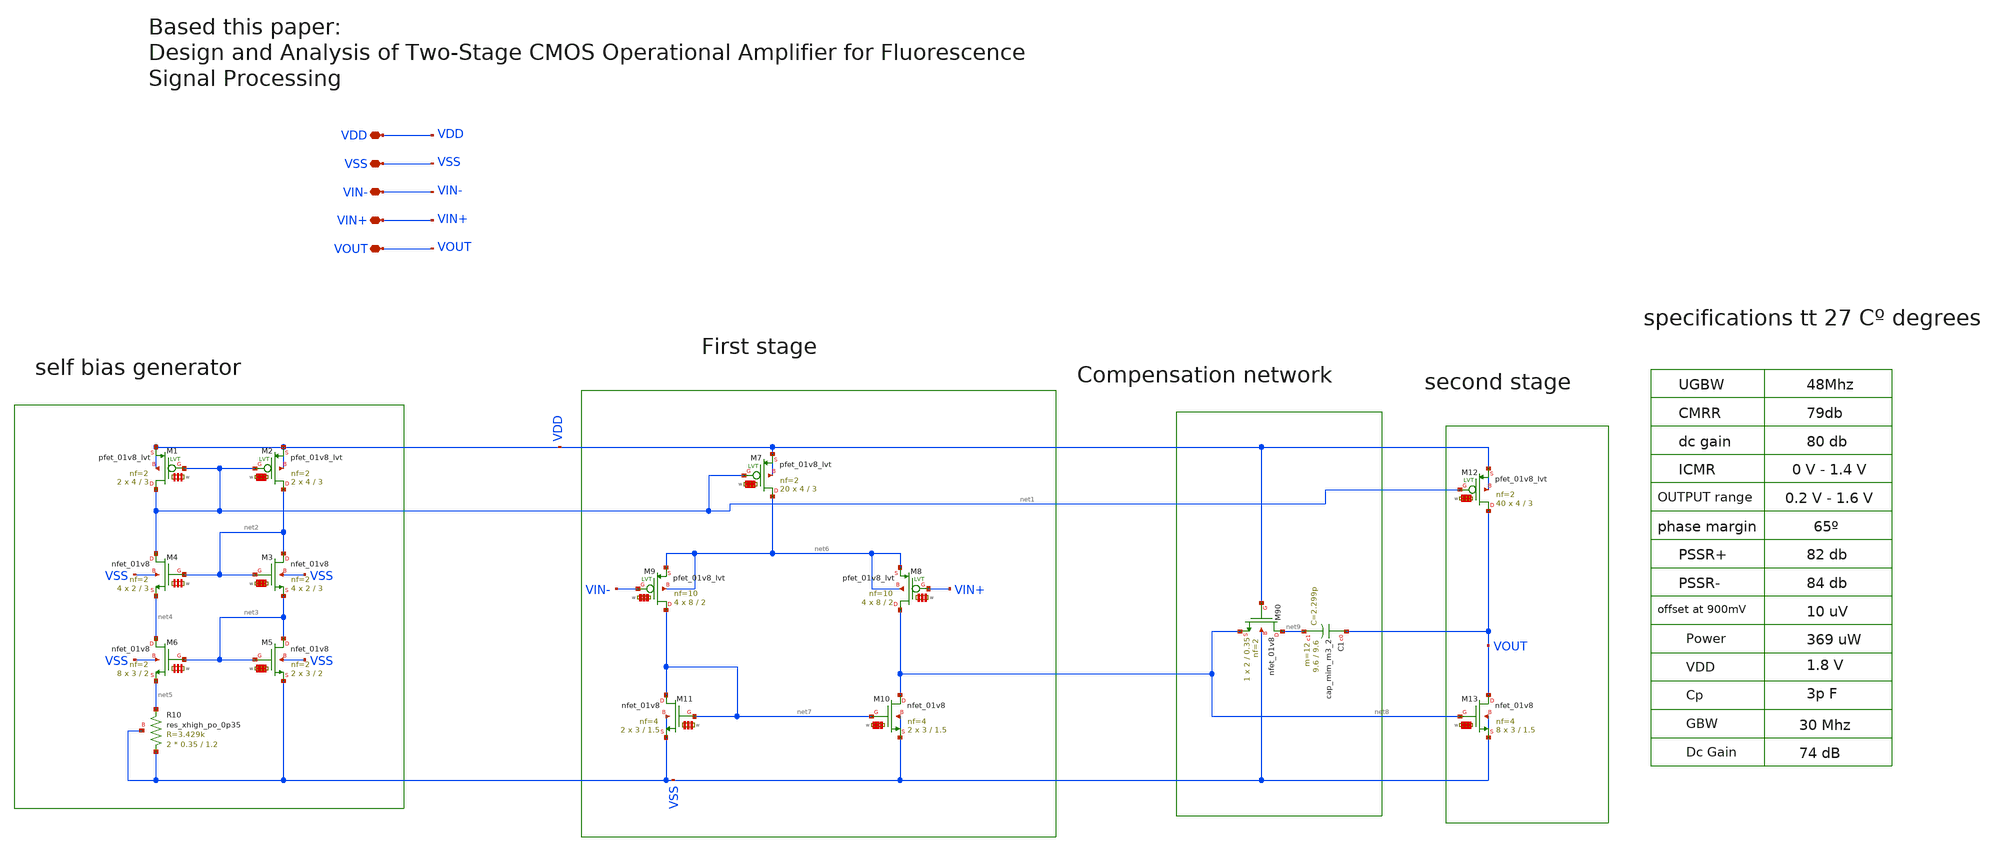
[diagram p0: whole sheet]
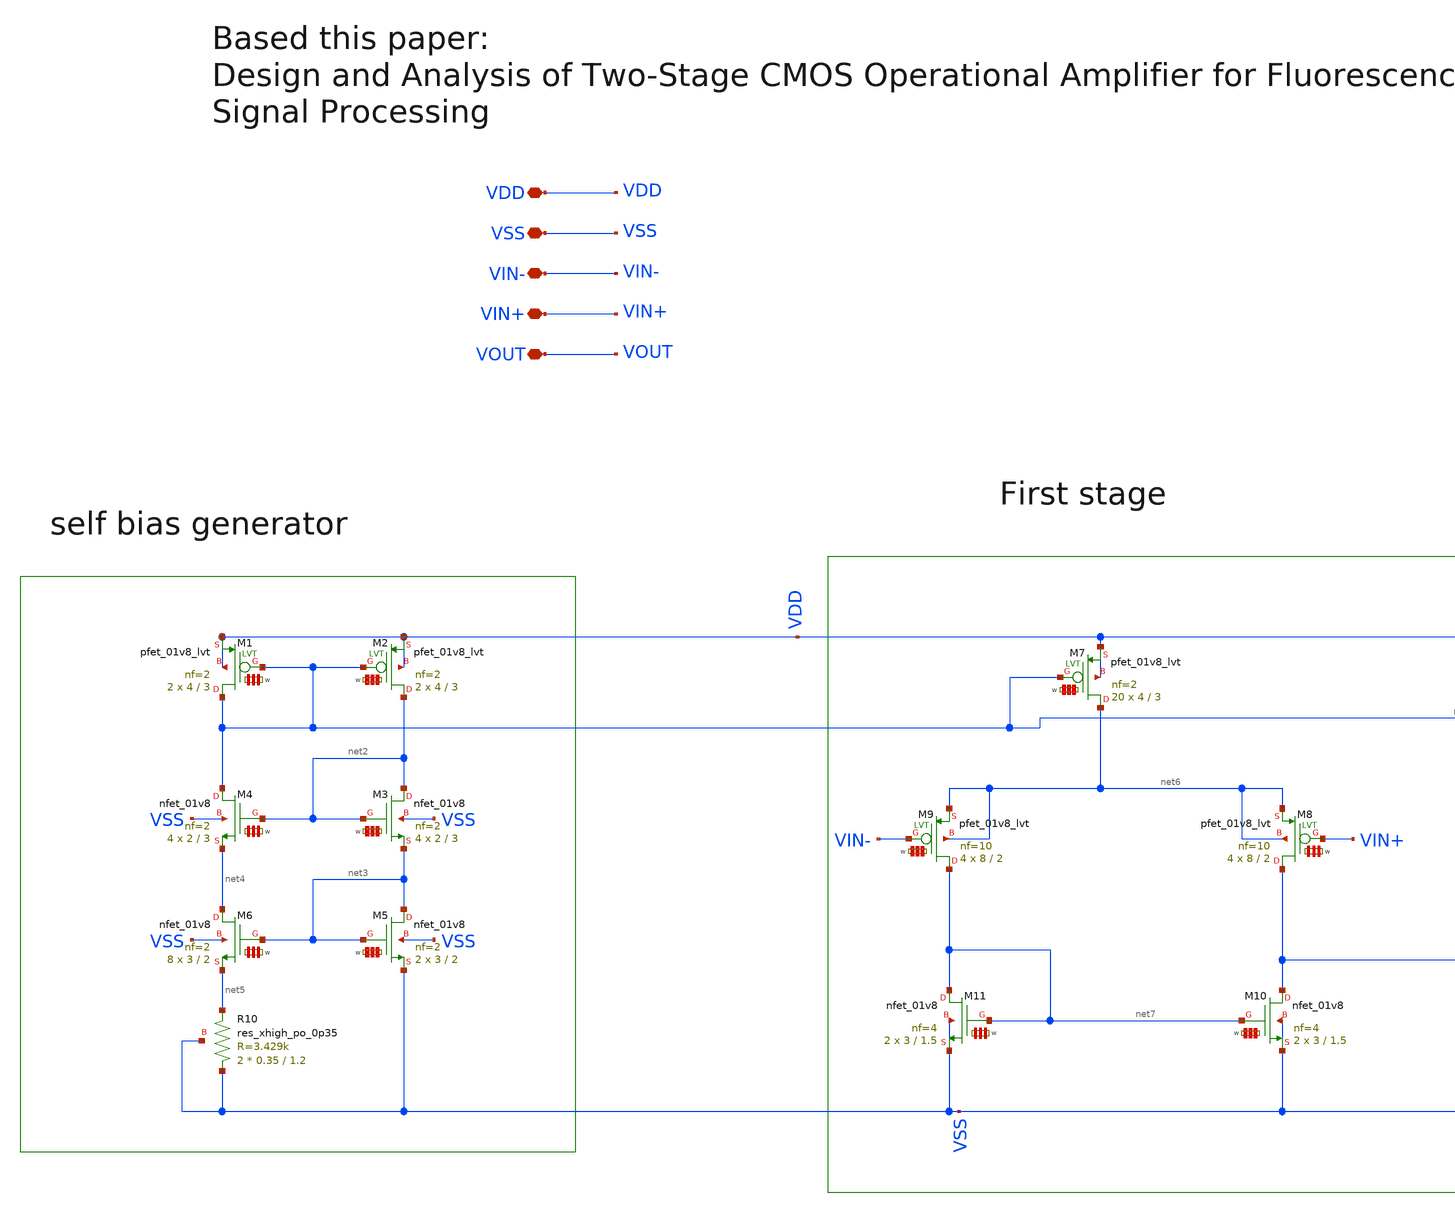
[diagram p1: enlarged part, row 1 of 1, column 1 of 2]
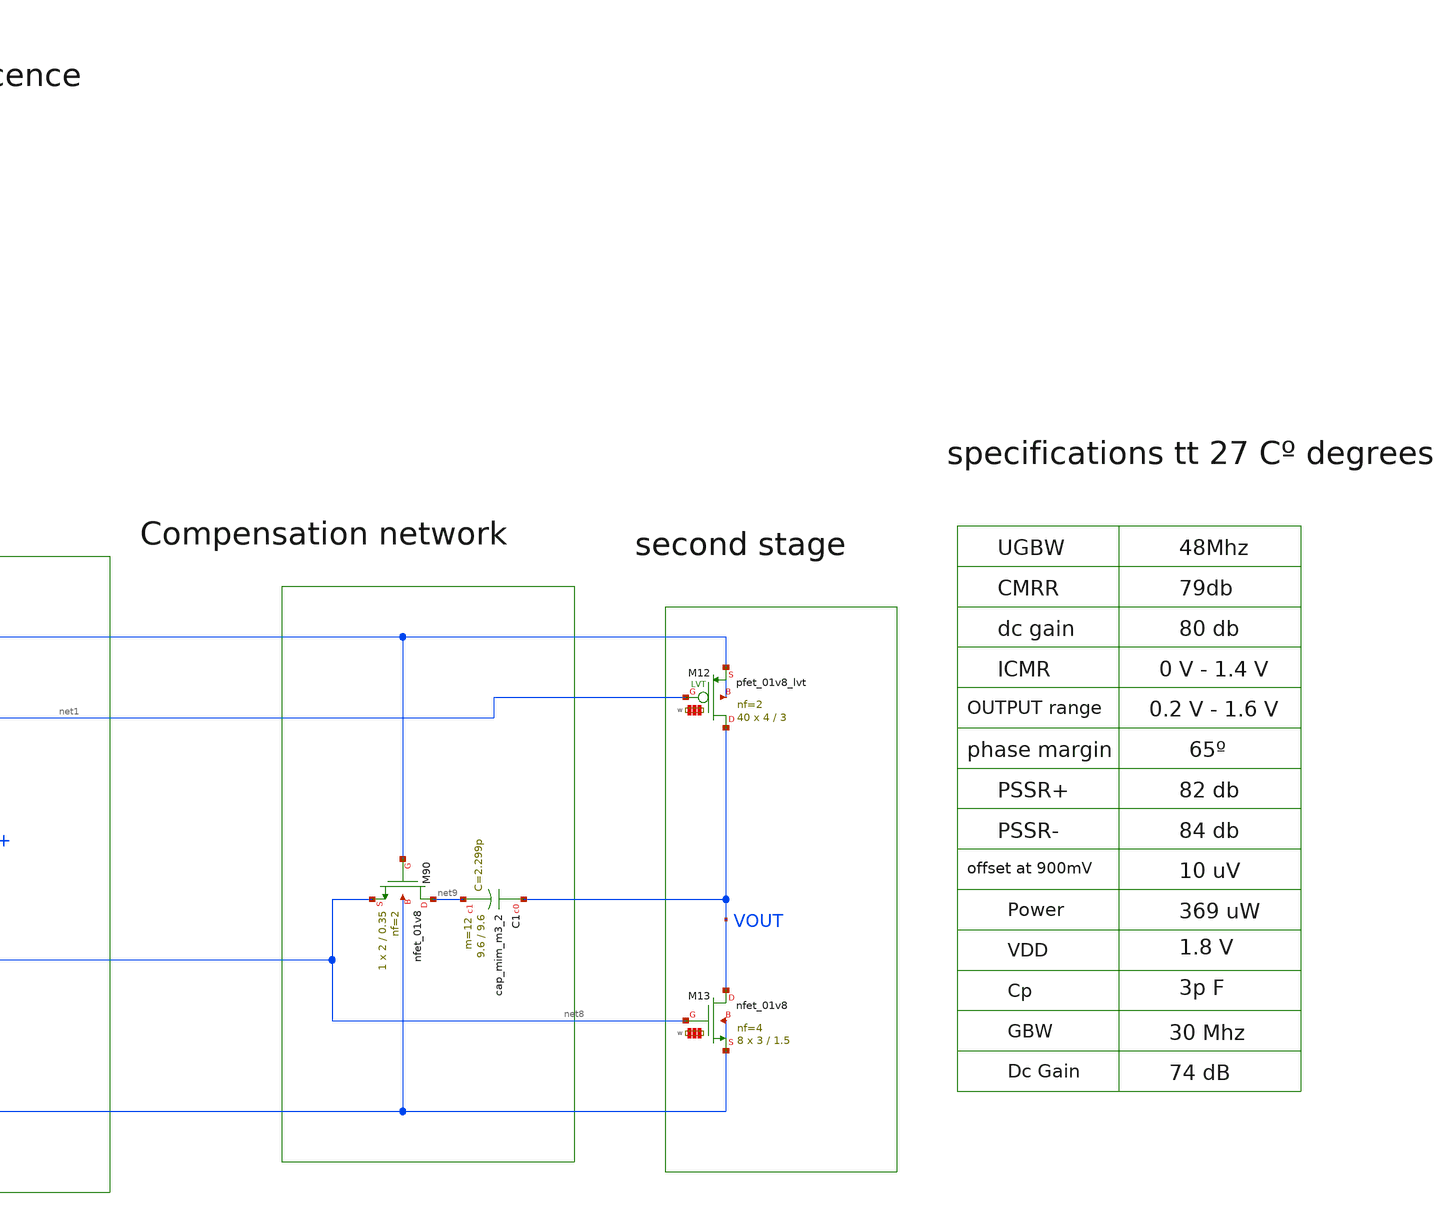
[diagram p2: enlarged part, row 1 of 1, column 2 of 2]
** sch_path: my_ip/LIB/Sky130A/single ended amplifiers/VA001_PMOS_1.8_sky130A.sch
**.subckt VA001_PMOS_1.8_sky130A VDD VSS VIN- VIN+ VOUT
*.iopin VDD
*.iopin VSS
*.iopin VIN-
*.iopin VIN+
*.iopin VOUT
XR10 VSS net5 VSS sky130_fd_pr__res_xhigh_po_0p35 L=1.2 mult=2 m=2
XM4 net1 net2 net4 VSS sky130_fd_pr__nfet_01v8 L=3 W='2 * 2 ' nf=2 ad='int((2 + 1)/2) * 2 / 2 * 0.29'
+ as='int((2 + 2)/2) * 2 / 2 * 0.29' pd='2*int((2 + 1)/2) * (2 / 2 + 0.29)' ps='2*int((2 + 2)/2) * (2 / 2 + 0.29)'
+ nrd='0.29 / 2 ' nrs='0.29 / 2 ' sa=0 sb=0 sd=0 mult=4 m=4
XM3 net2 net2 net3 VSS sky130_fd_pr__nfet_01v8 L=3 W='2 * 2 ' nf=2 ad='int((2 + 1)/2) * 2 / 2 * 0.29'
+ as='int((2 + 2)/2) * 2 / 2 * 0.29' pd='2*int((2 + 1)/2) * (2 / 2 + 0.29)' ps='2*int((2 + 2)/2) * (2 / 2 + 0.29)'
+ nrd='0.29 / 2 ' nrs='0.29 / 2 ' sa=0 sb=0 sd=0 mult=4 m=4
XM10 net8 net7 VSS VSS sky130_fd_pr__nfet_01v8 L=1.5 W='3 * 4 ' nf=4 ad='int((4 + 1)/2) * 3 / 4 * 0.29'
+ as='int((4 + 2)/2) * 3 / 4 * 0.29' pd='2*int((4 + 1)/2) * (3 / 4 + 0.29)' ps='2*int((4 + 2)/2) * (3 / 4 + 0.29)'
+ nrd='0.29 / 3 ' nrs='0.29 / 3 ' sa=0 sb=0 sd=0 mult=2 m=2
XM11 net7 net7 VSS VSS sky130_fd_pr__nfet_01v8 L=1.5 W='3 * 4 ' nf=4 ad='int((4 + 1)/2) * 3 / 4 * 0.29'
+ as='int((4 + 2)/2) * 3 / 4 * 0.29' pd='2*int((4 + 1)/2) * (3 / 4 + 0.29)' ps='2*int((4 + 2)/2) * (3 / 4 + 0.29)'
+ nrd='0.29 / 3 ' nrs='0.29 / 3 ' sa=0 sb=0 sd=0 mult=2 m=2
XM13 VOUT net8 VSS VSS sky130_fd_pr__nfet_01v8 L=1.5 W='3 * 4 ' nf=4 ad='int((4 + 1)/2) * 3 / 4 * 0.29'
+ as='int((4 + 2)/2) * 3 / 4 * 0.29' pd='2*int((4 + 1)/2) * (3 / 4 + 0.29)' ps='2*int((4 + 2)/2) * (3 / 4 + 0.29)'
+ nrd='0.29 / 3 ' nrs='0.29 / 3 ' sa=0 sb=0 sd=0 mult=8 m=8
XC1 VOUT net9 sky130_fd_pr__cap_mim_m3_2 W=9.6 L=9.6 MF=12 m=12
XM9 net7 VIN- net6 net6 sky130_fd_pr__pfet_01v8_lvt L=2 W='8 * 10 ' nf=10 ad='int((10 + 1)/2) * 8 / 10 * 0.29'
+ as='int((10 + 2)/2) * 8 / 10 * 0.29' pd='2*int((10 + 1)/2) * (8 / 10 + 0.29)' ps='2*int((10 + 2)/2) * (8 / 10 + 0.29)'
+ nrd='0.29 / 8 ' nrs='0.29 / 8 ' sa=0 sb=0 sd=0 mult=4 m=4
XM8 net8 VIN+ net6 net6 sky130_fd_pr__pfet_01v8_lvt L=2 W='8 * 10 ' nf=10 ad='int((10 + 1)/2) * 8 / 10 * 0.29'
+ as='int((10 + 2)/2) * 8 / 10 * 0.29' pd='2*int((10 + 1)/2) * (8 / 10 + 0.29)' ps='2*int((10 + 2)/2) * (8 / 10 + 0.29)'
+ nrd='0.29 / 8 ' nrs='0.29 / 8 ' sa=0 sb=0 sd=0 mult=4 m=4
XM90 net9 VDD net8 VSS sky130_fd_pr__nfet_01v8 L=0.35 W=2 nf=2 ad='int((2 + 1)/2) * 2 / 2 * 0.29' as='int((2 + 2)/2) * 2 / 2 * 0.29'
+ pd='2*int((2 + 1)/2) * (2 / 2 + 0.29)' ps='2*int((2 + 2)/2) * (2 / 2 + 0.29)' nrd='0.29 / 2 ' nrs='0.29 / 2 '
+ sa=0 sb=0 sd=0 mult=1 m=1
XM6 net4 net3 net5 VSS sky130_fd_pr__nfet_01v8 L=2 W='3 * 2 ' nf=2 ad='int((2 + 1)/2) * 3 / 2 * 0.29'
+ as='int((2 + 2)/2) * 3 / 2 * 0.29' pd='2*int((2 + 1)/2) * (3 / 2 + 0.29)' ps='2*int((2 + 2)/2) * (3 / 2 + 0.29)'
+ nrd='0.29 / 3 ' nrs='0.29 / 3 ' sa=0 sb=0 sd=0 mult=8 m=8
XM5 net3 net3 VSS VSS sky130_fd_pr__nfet_01v8 L=2 W='3 * 2 ' nf=2 ad='int((2 + 1)/2) * 3 / 2 * 0.29'
+ as='int((2 + 2)/2) * 3 / 2 * 0.29' pd='2*int((2 + 1)/2) * (3 / 2 + 0.29)' ps='2*int((2 + 2)/2) * (3 / 2 + 0.29)'
+ nrd='0.29 / 3 ' nrs='0.29 / 3 ' sa=0 sb=0 sd=0 mult=2 m=2
XM2 net2 net1 VDD VDD sky130_fd_pr__pfet_01v8_lvt L=3 W='4 * 2 ' nf=2 ad='int((2 + 1)/2) * 4 / 2 * 0.29'
+ as='int((2 + 2)/2) * 4 / 2 * 0.29' pd='2*int((2 + 1)/2) * (4 / 2 + 0.29)' ps='2*int((2 + 2)/2) * (4 / 2 + 0.29)'
+ nrd='0.29 / 4 ' nrs='0.29 / 4 ' sa=0 sb=0 sd=0 mult=2 m=2
XM1 net1 net1 VDD VDD sky130_fd_pr__pfet_01v8_lvt L=3 W='4 * 2 ' nf=2 ad='int((2 + 1)/2) * 4 / 2 * 0.29'
+ as='int((2 + 2)/2) * 4 / 2 * 0.29' pd='2*int((2 + 1)/2) * (4 / 2 + 0.29)' ps='2*int((2 + 2)/2) * (4 / 2 + 0.29)'
+ nrd='0.29 / 4 ' nrs='0.29 / 4 ' sa=0 sb=0 sd=0 mult=2 m=2
XM7 net6 net1 VDD VDD sky130_fd_pr__pfet_01v8_lvt L=3 W='4 * 2 ' nf=2 ad='int((2 + 1)/2) * 4 / 2 * 0.29'
+ as='int((2 + 2)/2) * 4 / 2 * 0.29' pd='2*int((2 + 1)/2) * (4 / 2 + 0.29)' ps='2*int((2 + 2)/2) * (4 / 2 + 0.29)'
+ nrd='0.29 / 4 ' nrs='0.29 / 4 ' sa=0 sb=0 sd=0 mult=20 m=20
XM12 VOUT net1 VDD VDD sky130_fd_pr__pfet_01v8_lvt L=3 W='4 * 2 ' nf=2 ad='int((2 + 1)/2) * 4 / 2 * 0.29'
+ as='int((2 + 2)/2) * 4 / 2 * 0.29' pd='2*int((2 + 1)/2) * (4 / 2 + 0.29)' ps='2*int((2 + 2)/2) * (4 / 2 + 0.29)'
+ nrd='0.29 / 4 ' nrs='0.29 / 4 ' sa=0 sb=0 sd=0 mult=40 m=40
**.ends
.end
